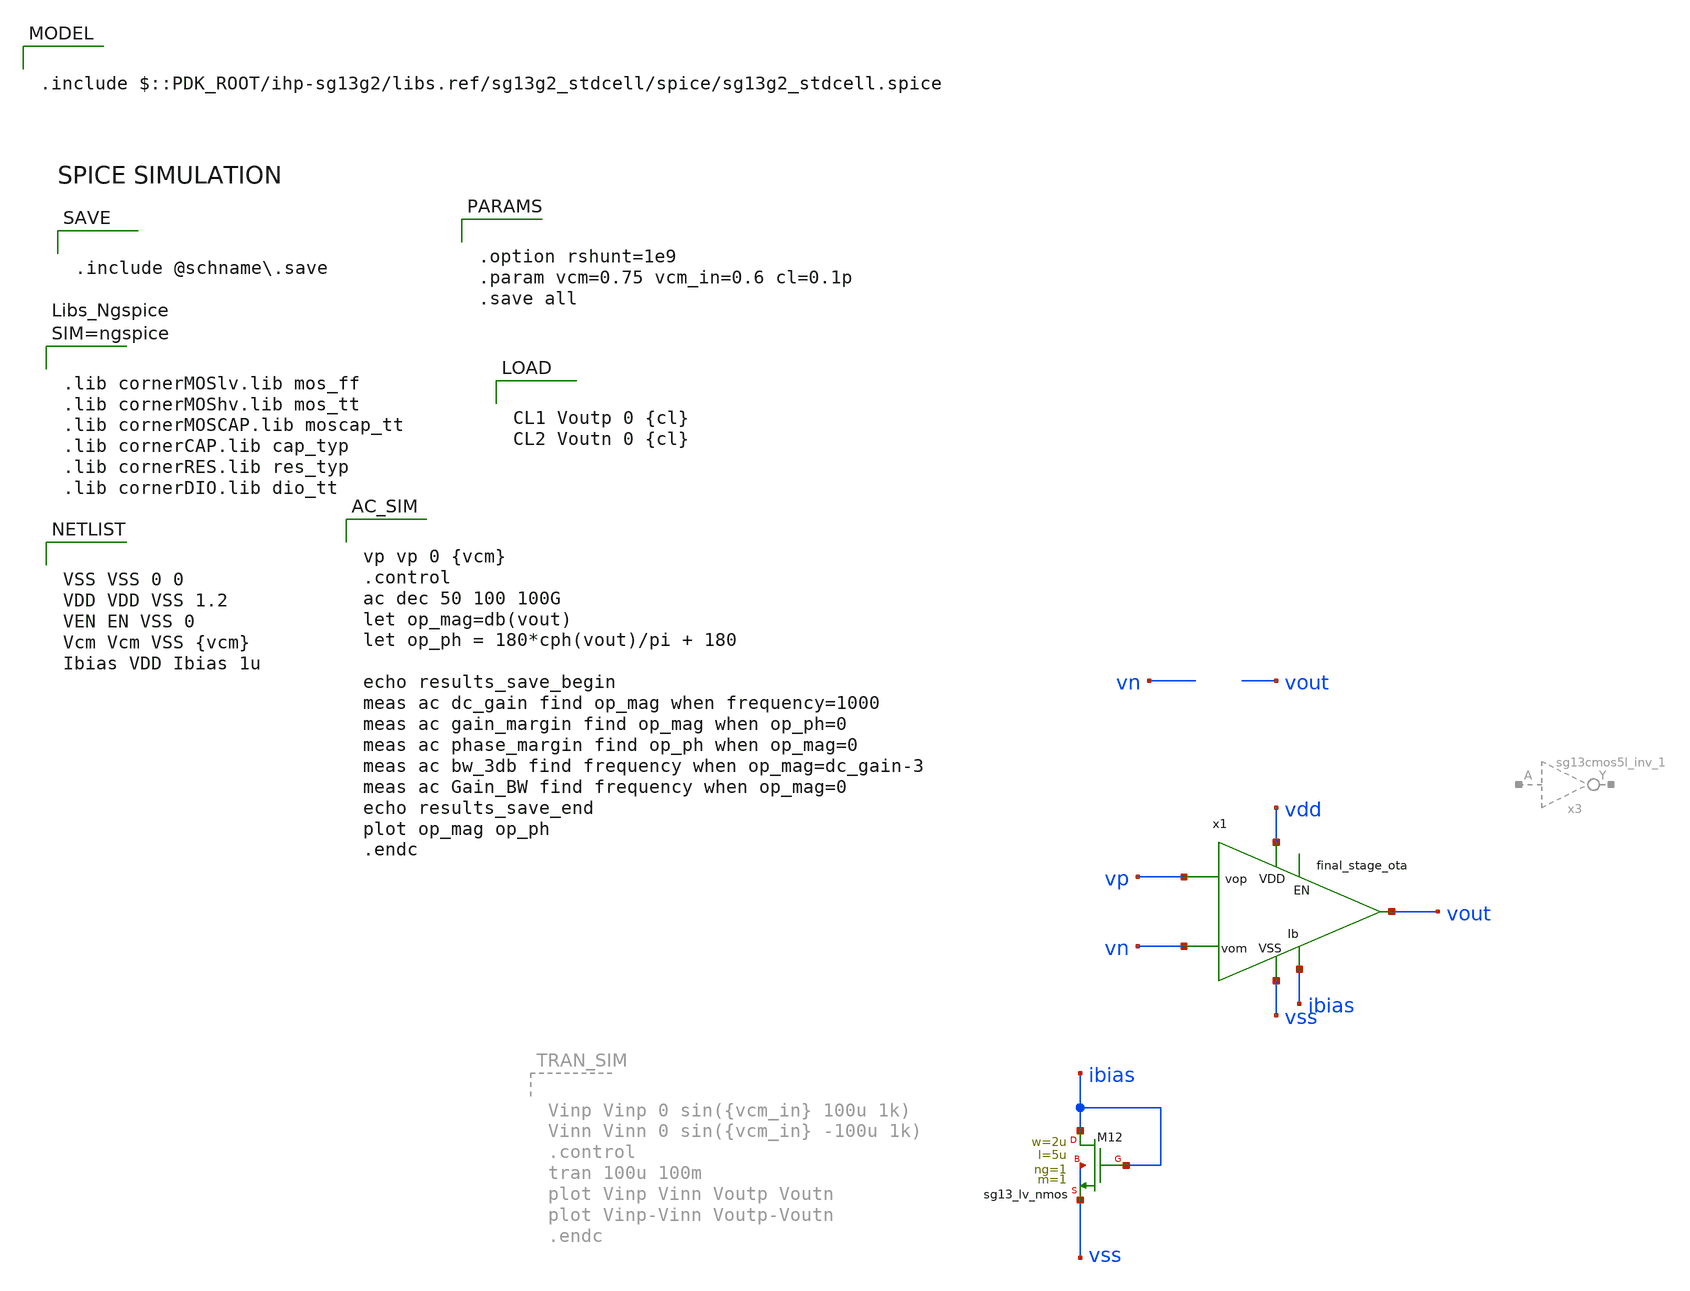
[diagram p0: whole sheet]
** sch_path: schematic/xschem/final_stage_ota/final_stage_ota_tb.sch

.include $::PDK_ROOT/ihp-sg13g2/libs.ref/sg13g2_stdcell/spice/sg13g2_stdcell.spice


**.subckt final_stage_ota_tb
x1 vdd ibias vp vn vout vss final_stage_ota
XM12 ibias ibias vss vss sg13_lv_nmos w=2u l=5u ng=1 m=1 mm_ok=1
**** begin user architecture code


VSS VSS 0 0
VDD VDD VSS 1.2
VEN EN VSS 0
Vcm Vcm VSS {vcm}
Ibias VDD Ibias 1u



.control
op
let ro_n = voutn/i(vmeas2)
let ro_p = voutp/i(vmeas3)
print ro_n ro_p
write @schname.raw
.endc




.lib cornerMOSlv.lib mos_ff
.lib cornerMOShv.lib mos_tt
.lib cornerMOSCAP.lib moscap_tt
.lib cornerCAP.lib cap_typ
.lib cornerRES.lib res_typ
.lib cornerDIO.lib dio_tt





vp vp 0 {vcm}
.control
ac dec 50 100 100G
let op_mag=db(vout)
let op_ph = 180*cph(vout)/pi + 180

echo results_save_begin
meas ac dc_gain find op_mag when frequency=1000
meas ac gain_margin find op_mag when op_ph=0
meas ac phase_margin find op_ph when op_mag=0
meas ac bw_3db find frequency when op_mag=dc_gain-3
meas ac Gain_BW find frequency when op_mag=0
echo results_save_end
plot op_mag op_ph
.endc




.option rshunt=1e9
.param vcm=0.75 vcm_in=0.6 cl=0.1p
.save all




CL1 Voutp 0 {cl}
CL2 Voutn 0 {cl}



.include @schname.save

**** end user architecture code
**.ends

* expanding   symbol:  /foss/designs/ic_design/chipaloza/schema/final_stage_ota/final_stage_ota.sym
*+ # of pins=6
** sym_path: schematic/xschem/final_stage_ota/final_stage_ota.sym
** sch_path: schematic/xschem/final_stage_ota/final_stage_ota.sch
.subckt final_stage_ota vdd iout vop vom vout vss
*.iopin vdd
*.iopin vom
*.iopin vop
*.iopin vss
*.iopin vout
*.iopin iout
XM1 vdd ibp vt vdd sg13_lv_pmos w=1u l=3u ng=1 m=2 mm_ok=1
XM2 net1 net1 vss vss sg13_lv_nmos w=0.15u l=3u ng=1 m=2 mm_ok=1
XM3 vt vom net1 vdd sg13_lv_pmos w=3.12u l=1u ng=1 m=2 mm_ok=1
XM4 vout net1 vss vss sg13_lv_nmos w=0.15u l=3u ng=1 m=2 mm_ok=1
XM5 vt vop vout vdd sg13_lv_pmos w=3.12u l=1u ng=1 m=2 mm_ok=1
XM6 ibp iout vss vss sg13_lv_nmos w=2u l=5u ng=1 m=1 mm_ok=1
XM7 vdd ibp ibp vdd sg13_lv_pmos w=1u l=3u ng=1 m=1 mm_ok=1
.ends

.end
